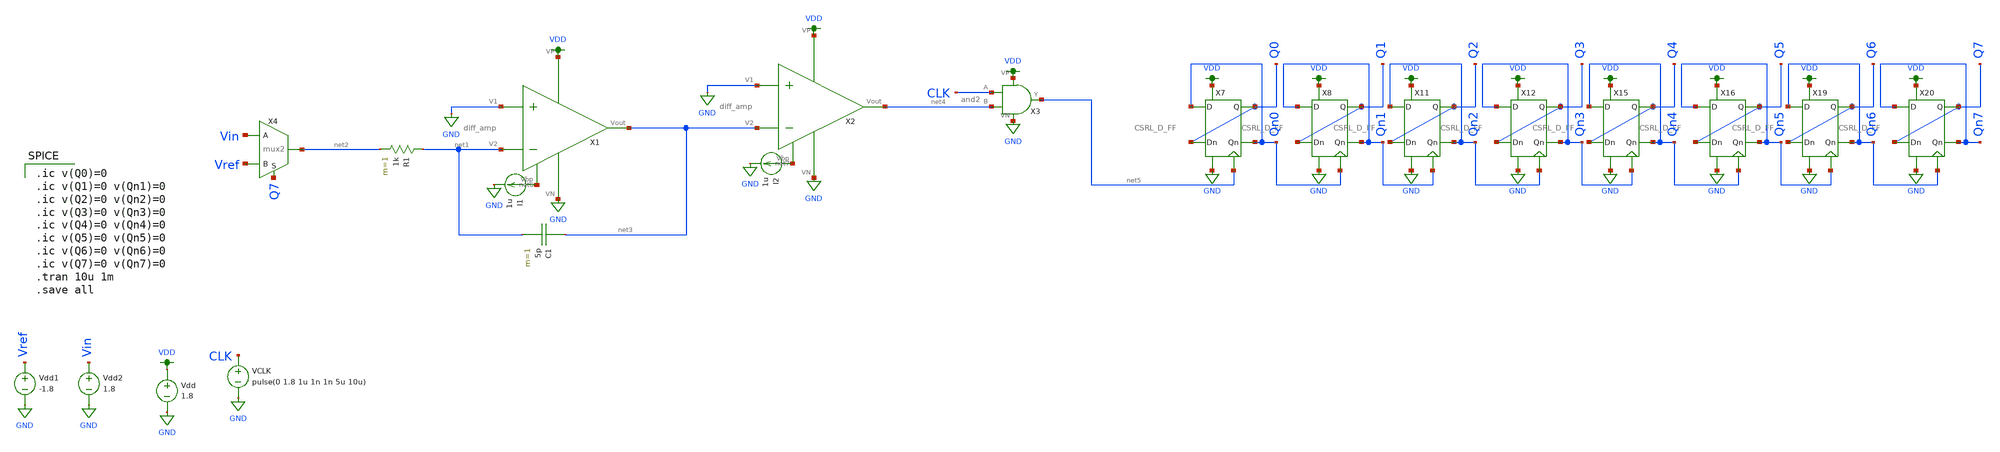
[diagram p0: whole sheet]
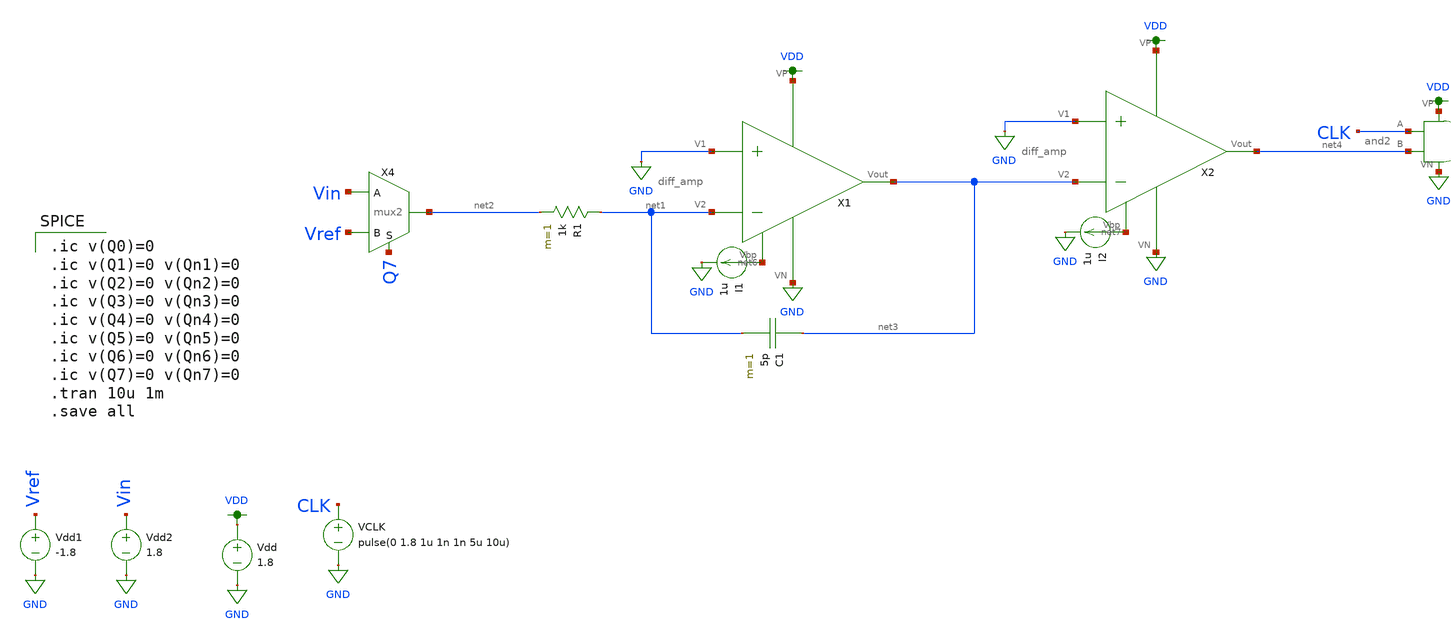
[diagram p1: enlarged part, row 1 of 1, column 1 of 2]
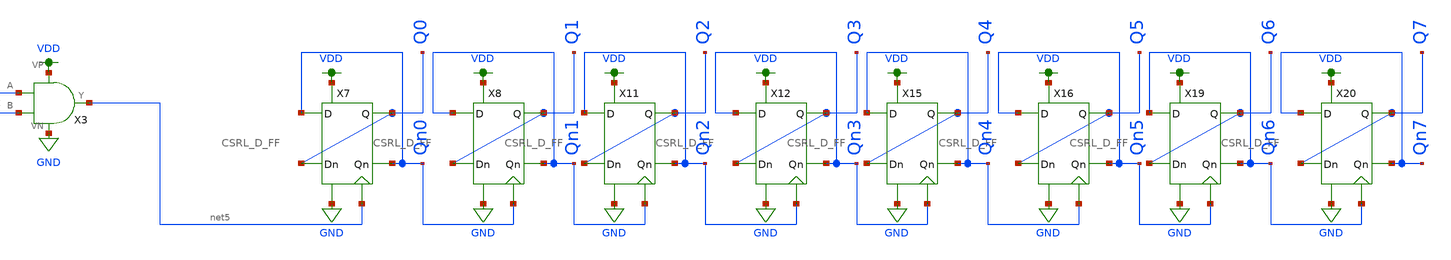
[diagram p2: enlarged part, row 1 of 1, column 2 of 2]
** sch_path: schematic/double-slope.sch
**.subckt double-slope
X1 VDD net6 net3 GND net1 GND diff_amp
X2 VDD net7 net4 GND net3 GND diff_amp
X3 VDD CLK GND net5 net4 and2
R1 net1 net2 1k m=1
C1 net3 net1 5p m=1
Vdd VDD GND 1.8
VCLK CLK GND pulse(0 1.8 1u 1n 1n 5u 10u)
Vdd1 Vref GND -1.8
Vdd2 Vin GND 1.8
X4 net2 Vin Vref Q7 mux2
X7 Q0 Qn0 Qn0 Q0 GND VDD net5 CSRL_D_FF
X8 Q1 Qn1 Qn1 Q1 GND VDD Qn0 CSRL_D_FF
X11 Q2 Qn2 Qn2 Q2 GND VDD Qn1 CSRL_D_FF
X12 Q3 Qn3 Qn3 Q3 GND VDD Qn2 CSRL_D_FF
X15 Q4 Qn4 Qn4 Q4 GND VDD Qn3 CSRL_D_FF
X16 Q5 Qn5 Qn5 Q5 GND VDD Qn4 CSRL_D_FF
X19 Q6 Qn6 Qn6 Q6 GND VDD Qn5 CSRL_D_FF
X20 Q7 Qn7 Qn7 Q7 GND VDD Qn6 CSRL_D_FF
I1 net6 GND 1u
I2 net7 GND 1u
**** begin user architecture code

.option wnflag=1
.param MC_SWITCH=0.0
.lib ~/skywater/skywater-pdk/libraries/sky130_fd_pr_ngspice/latest/models/sky130.lib.spice tt


.ic v(Q0)=0
.ic v(Q1)=0 v(Qn1)=0
.ic v(Q2)=0 v(Qn2)=0
.ic v(Q3)=0 v(Qn3)=0
.ic v(Q4)=0 v(Qn4)=0
.ic v(Q5)=0 v(Qn5)=0
.ic v(Q6)=0 v(Qn6)=0
.ic v(Q7)=0 v(Qn7)=0
.tran 10u 1m
.save all

**** end user architecture code
**.ends
.GLOBAL GND
.GLOBAL VDD
.end
